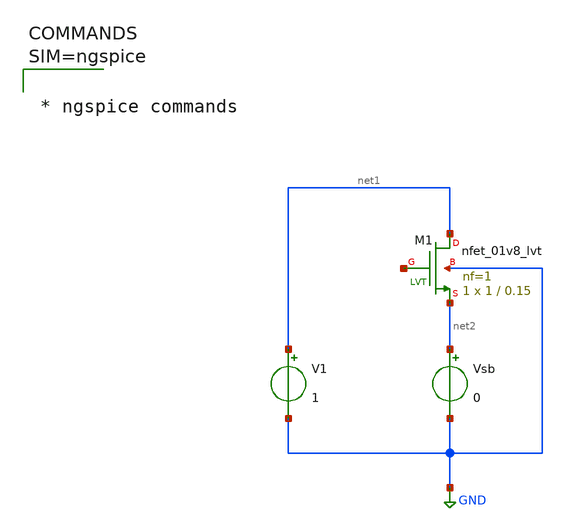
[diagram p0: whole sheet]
** sch_path: xschem/untitled.sch
**.subckt untitled
XM1 net1 net3 net2 GND sky130_fd_pr__nfet_01v8_lvt L=0.15 W=1 nf=1 ad='int((1 + 1)/2) * 1 / 1 * 0.29'
+ as='int((1 + 2)/2) * 1 / 1 * 0.29' pd='2*int((1 + 1)/2) * (1 / 1 + 0.29)' ps='2*int((1 + 2)/2) * (1 / 1 + 0.29)'
+ nrd='0.29 / 1 ' nrs='0.29 / 1 ' sa=0 sb=0 sd=0 mult=1 m=1
V1 net1 GND 1
Vsb net2 GND 0
**** begin user architecture code



* ngspice commands



**** end user architecture code
**.ends
.GLOBAL GND
.end
